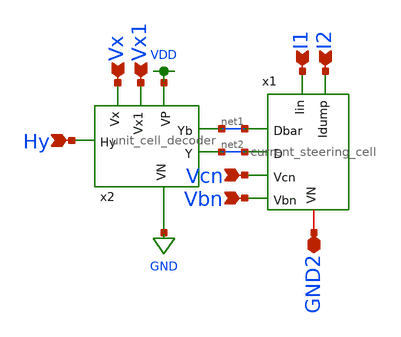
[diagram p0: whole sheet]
** sch_path: lvs/unit_cell_for_lvs.sch
**.subckt unit_cell_for_lvs Vx Vx1 Hy I1 I2 Vcn Vbn GND2
*.ipin Vx
*.ipin Vx1
*.ipin Hy
*.ipin I1
*.ipin I2
*.ipin Vcn
*.ipin Vbn
*.iopin GND2
x1 I1 I2 net1 net2 Vcn Vbn GND2 current_steering_cell
x2 Vx Vx1 Hy VDD GND net1 net2 unit_cell_decoder
**.ends
.GLOBAL VDD
.GLOBAL GND
.end
